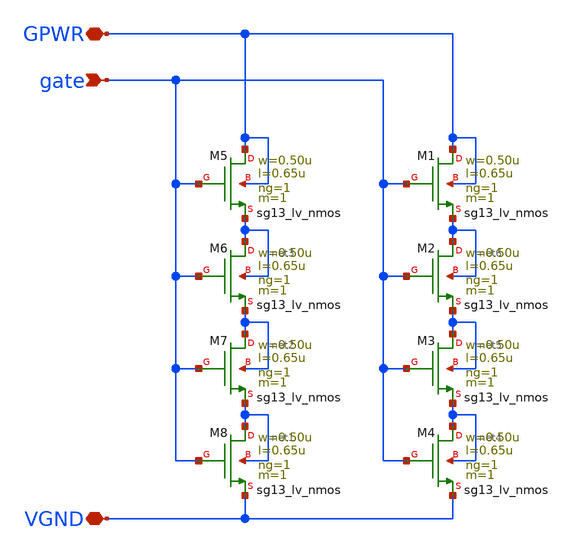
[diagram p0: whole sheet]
** sch_path: ihp-sg13cmos5l/libs.tech/xschem/hm_analog/dischg.sch
**.subckt dischg GPWR VGND gate
*.iopin GPWR
*.iopin VGND
*.ipin gate
XM1 GPWR gate net6 GPWR sg13_lv_nmos w=0.50u l=0.65u ng=1 m=1 mm_ok=1
XM2 net6 gate net5 net6 sg13_lv_nmos w=0.50u l=0.65u ng=1 m=1 mm_ok=1
XM3 net5 gate net4 net5 sg13_lv_nmos w=0.50u l=0.65u ng=1 m=1 mm_ok=1
XM4 net4 gate VGND net4 sg13_lv_nmos w=0.50u l=0.65u ng=1 m=1 mm_ok=1
XM5 GPWR gate net3 GPWR sg13_lv_nmos w=0.50u l=0.65u ng=1 m=1 mm_ok=1
XM6 net3 gate net2 net3 sg13_lv_nmos w=0.50u l=0.65u ng=1 m=1 mm_ok=1
XM7 net2 gate net1 net2 sg13_lv_nmos w=0.50u l=0.65u ng=1 m=1 mm_ok=1
XM8 net1 gate VGND net1 sg13_lv_nmos w=0.50u l=0.65u ng=1 m=1 mm_ok=1
**.ends
.end
